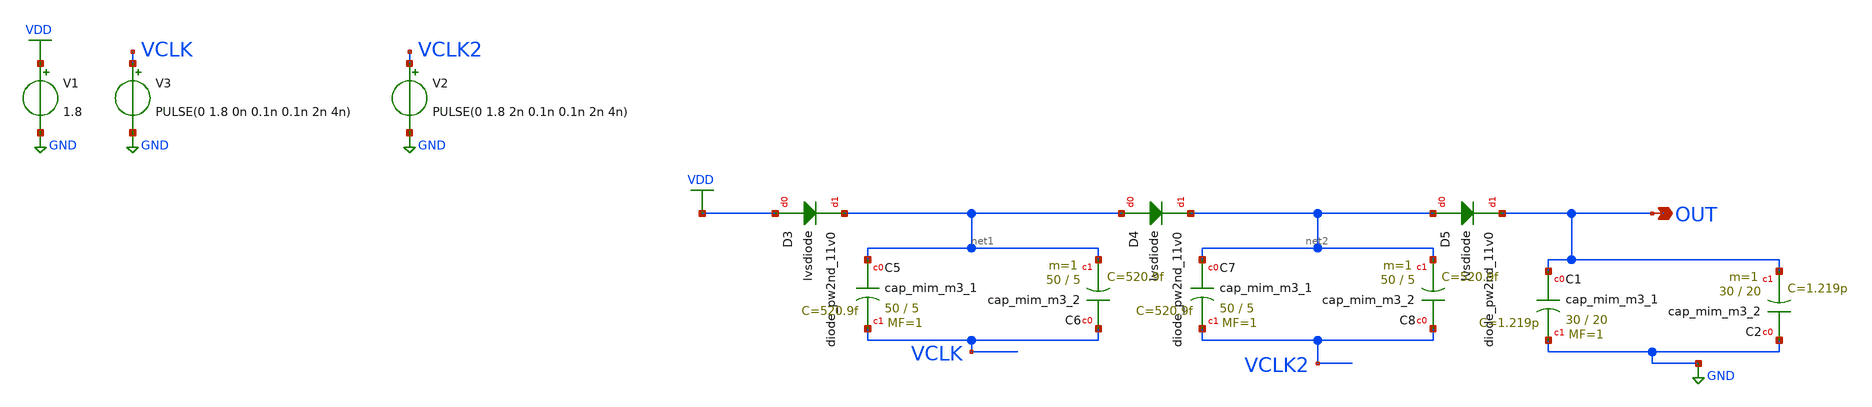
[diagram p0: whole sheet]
** sch_path: sky130_cells/ChargePump/twostagePump_TB.sch
**.subckt twostagePump_TB OUT
*.opin OUT
V3 VCLK GND PULSE(0 1.8 0n 0.1n 0.1n 2n 4n)
V1 VDD GND 1.8
V2 VCLK2 GND PULSE(0 1.8 2n 0.1n 0.1n 2n 4n)
D3 VDD net1 sky130_fd_pr__diode_pw2nd_11v0 area=50
D4 net1 net2 sky130_fd_pr__diode_pw2nd_11v0 area=50
D5 net2 OUT sky130_fd_pr__diode_pw2nd_11v0 area=50
XC5 net1 VCLK sky130_fd_pr__cap_mim_m3_1 W=50 L=5 MF=1 m=1
XC6 VCLK net1 sky130_fd_pr__cap_mim_m3_2 W=50 L=5 MF=1 m=1
XC7 net2 VCLK2 sky130_fd_pr__cap_mim_m3_1 W=50 L=5 MF=1 m=1
XC8 VCLK2 net2 sky130_fd_pr__cap_mim_m3_2 W=50 L=5 MF=1 m=1
XC1 OUT GND sky130_fd_pr__cap_mim_m3_1 W=30 L=20 MF=1 m=1
XC2 GND OUT sky130_fd_pr__cap_mim_m3_2 W=30 L=20 MF=1 m=1
**** begin user architecture code

** opencircuitdesign pdks install
.lib $::SKYWATER_MODELS/sky130.lib.spice tt




.tran 100p 60n
.save
.control
run
//wrdata     .txt V(out)
plot V(out) V(VCLK) V(VCLK2)

.endc
//V(Switch1)+1 V(Switch2)+1 V(Switch3)+1 V(Inn)+1.8


**** end user architecture code
**.ends
.GLOBAL GND
.GLOBAL VDD
.end
